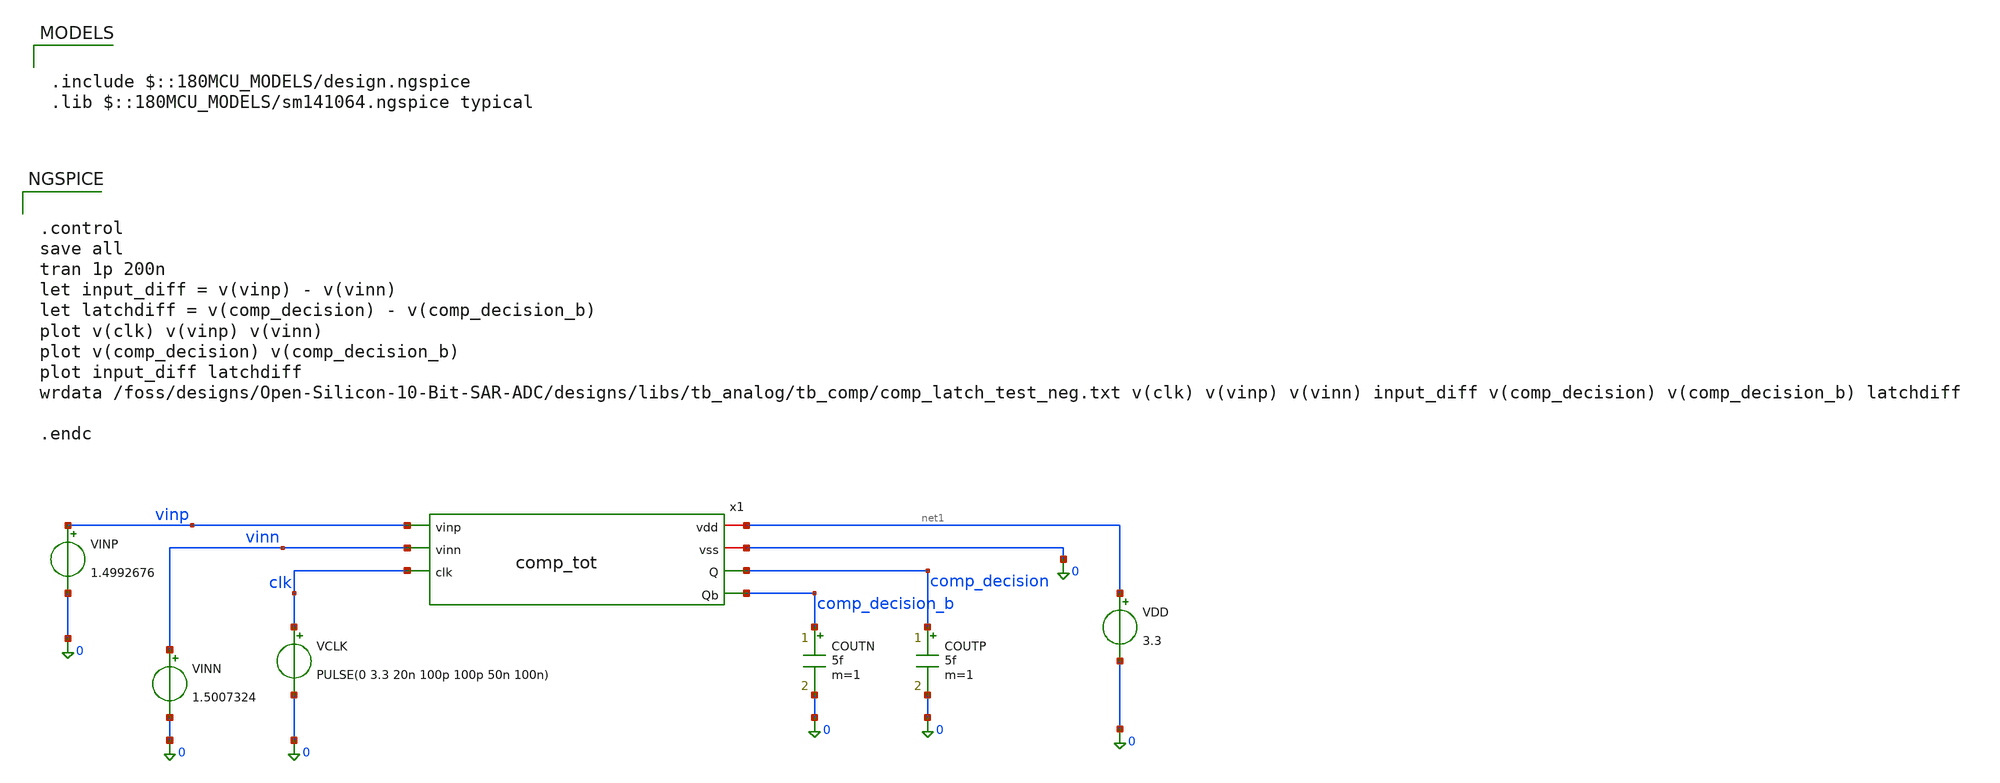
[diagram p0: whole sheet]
** sch_path: designs/libs/tb_analog/comp_tot_tb.sch
**.subckt comp_tot_tb
VCLK clk 0 PULSE(0 3.3 20n 100p 100p 50n 100n)
VINP vinp 0 1.4992676
VINN vinn 0 1.5007324
COUTP comp_decision 0 5f m=1
COUTN comp_decision_b 0 5f m=1
VDD net1 0 3.3
x1 vinp net1 vinn clk 0 comp_decision comp_decision_b comp_tot
**** begin user architecture code

.include $::180MCU_MODELS/design.ngspice
.lib $::180MCU_MODELS/sm141064.ngspice typical



.control
save all
tran 1p 200n
let input_diff = v(vinp) - v(vinn)
let latchdiff = v(comp_decision) - v(comp_decision_b)
plot v(clk) v(vinp) v(vinn)
plot v(comp_decision) v(comp_decision_b)
plot input_diff latchdiff
wrdata
+ /foss/designs/Open-Silicon-10-Bit-SAR-ADC/designs/libs/tb_analog/tb_comp/comp_latch_test_neg.txt v(clk) v(vinp) v(vinn) input_diff v(comp_decision) v(comp_decision_b) latchdiff

.endc


**** end user architecture code
**.ends
.end
